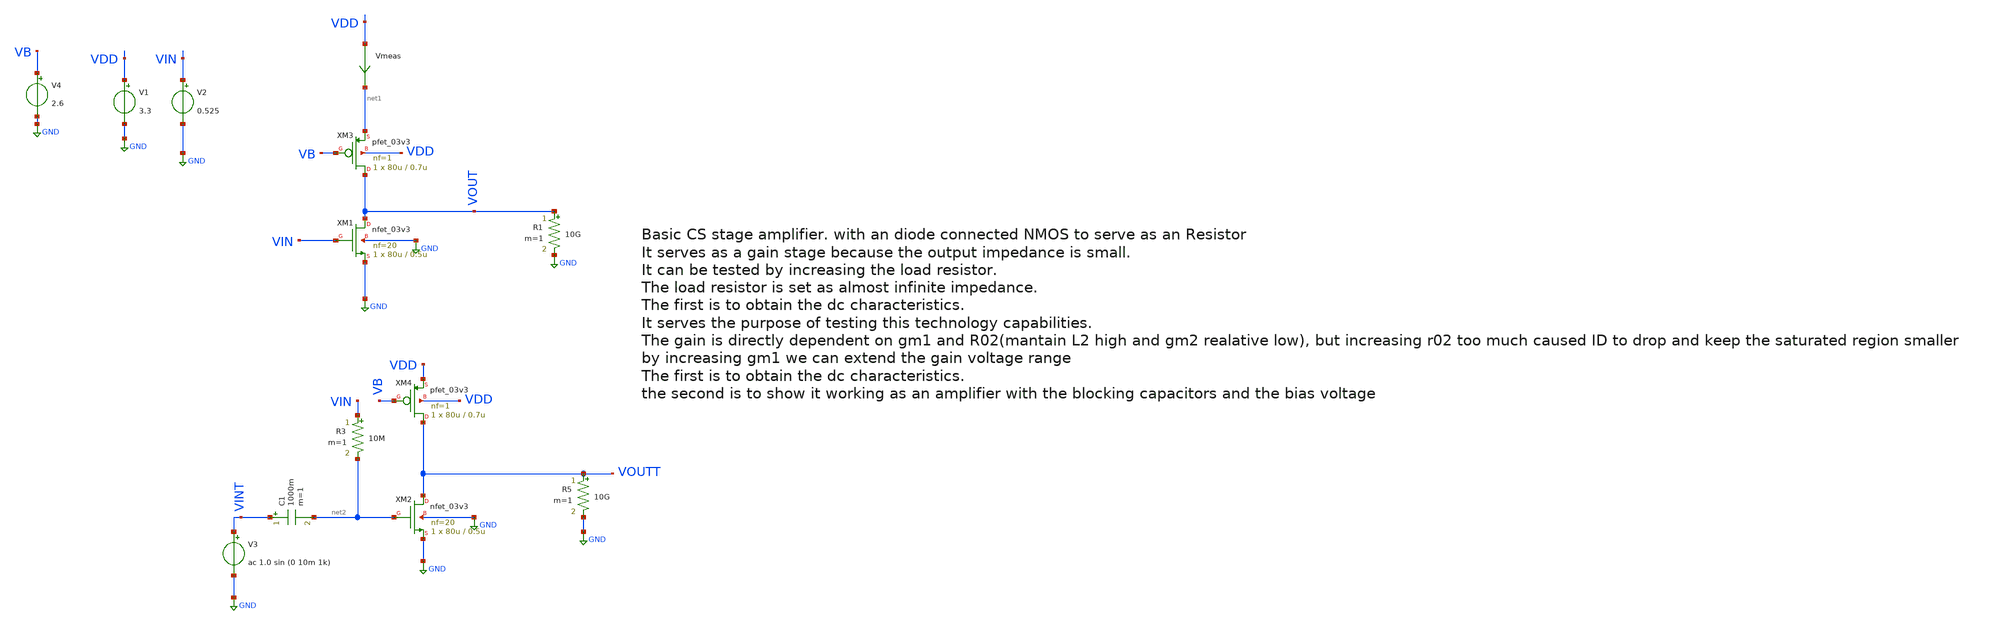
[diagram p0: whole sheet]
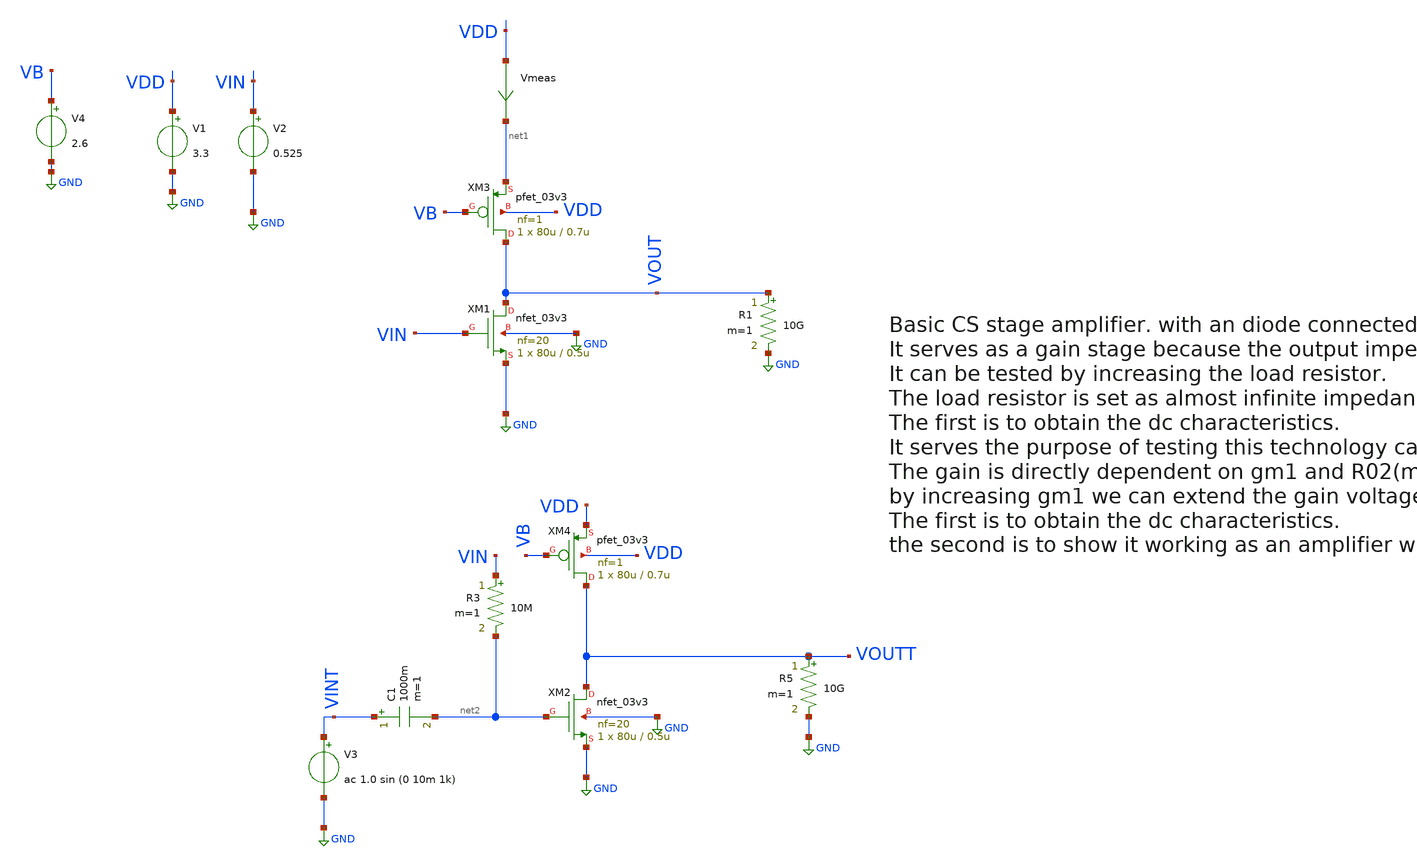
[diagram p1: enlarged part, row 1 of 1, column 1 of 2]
** sch_path: basic_circuits/cs_current_source_stage.sch
**.subckt cs_current_source_stage
XM1 VOUT VIN GND GND nfet_03v3 L=0.5u W=80u nf=20 ad='int((nf+1)/2) * W/nf * 0.18u' as='int((nf+2)/2) * W/nf * 0.18u'
+ pd='2*int((nf+1)/2) * (W/nf + 0.18u)' ps='2*int((nf+2)/2) * (W/nf + 0.18u)' nrd='0.18u / W' nrs='0.18u / W'
+ sa=0 sb=0 sd=0 m=1
Vmeas VDD net1 0
.save i(vmeas)
V1 VDD GND 3.3
V2 VIN GND 0.525
V3 VINT GND ac 1.0 sin (0 10m 1k)
C1 VINT net2 1000m m=1
R3 VIN net2 10M m=1
R5 VOUTT GND 10G m=1
XM2 VOUTT net2 GND GND nfet_03v3 L=0.5u W=80u nf=20 ad='int((nf+1)/2) * W/nf * 0.18u' as='int((nf+2)/2) * W/nf * 0.18u'
+ pd='2*int((nf+1)/2) * (W/nf + 0.18u)' ps='2*int((nf+2)/2) * (W/nf + 0.18u)' nrd='0.18u / W' nrs='0.18u / W'
+ sa=0 sb=0 sd=0 m=1
XM3 VOUT VB net1 VDD pfet_03v3 L=0.7u W=80u nf=1 ad='int((nf+1)/2) * W/nf * 0.18u' as='int((nf+2)/2) * W/nf * 0.18u'
+ pd='2*int((nf+1)/2) * (W/nf + 0.18u)' ps='2*int((nf+2)/2) * (W/nf + 0.18u)' nrd='0.18u / W' nrs='0.18u / W'
+ sa=0 sb=0 sd=0 m=1
V4 VB GND 2.6
XM4 VOUTT VB VDD VDD pfet_03v3 L=0.7u W=80u nf=1 ad='int((nf+1)/2) * W/nf * 0.18u' as='int((nf+2)/2) * W/nf * 0.18u'
+ pd='2*int((nf+1)/2) * (W/nf + 0.18u)' ps='2*int((nf+2)/2) * (W/nf + 0.18u)' nrd='0.18u / W' nrs='0.18u / W'
+ sa=0 sb=0 sd=0 m=1
R1 VOUT GND 10G m=1
**** begin user architecture code

**************************************************************
**************************************************************
**************************************************************
**************************************************************
**************************************************************
*LIBs*********************************************************
**************************************************************
**************************************************************
**************************************************************
**************************************************************
**************************************************************
.include $::180MCU_MODELS/design.ngspice
*.lib $::180MCU_MODELS/sm141064.ngspice statistical *use statistical if you want global and parameter mismatch
*.lib $::180MCU_MODELS/sm141064.ngspice res_statistical
.lib $::180MCU_MODELS/sm141064.ngspice typical
.lib $::180MCU_MODELS/sm141064.ngspice res_typical
.lib $::180MCU_MODELS/sm141064.ngspice moscap_typical
.lib $::180MCU_MODELS/sm141064.ngspice bjt_typical
.lib $::180MCU_MODELS/sm141064.ngspice diode_typical
.lib $::180MCU_MODELS/sm141064.ngspice mimcap_typical
**************************************************************
**************************************************************
**************************************************************
**************************************************************
**************************************************************
*Corners/montecarlo options***********************************
**************************************************************
**************************************************************
**************************************************************
**************************************************************
**************************************************************
.TEMP 27
.param   sw_stat_global = 1   sw_stat_mism = 1  mc_skew = 3  res_mc_skew = 3  cap_mc_skew = 3
+  fnoicor = 1
**************************************************************
**************************************************************
**************************************************************
**************************************************************
*SIMULATION and Plots*****************************************
**************************************************************
**************************************************************
**************************************************************
**************************************************************
.control
save all
dc V2 0 3.3 0.01
*dc simulation
plot v(VOUT) v(VIN) deriv(v(VOUT))
*ploting VIN VOUT and the voltage gain
plot i(Vmeas)
*ploting the current for curiosity
tran 100ns 2m
*transient simulation
plot (v(VINT)) (v(VOUTT)-1.700)
*simple plot to exemplify the gain
fft v(VOUTT) v(VINT)
*fast fourier transfor
plot mag(v(VOUTT)) mag(v(VINT))
* analyse the frequency spectrum of the transient waves, to detect distortion
ac dec 20 1 50G
*simple ac simulation
plot v(VOUTT)
*gain in function of the input frequency
.endc

**** end user architecture code
**.ends
.GLOBAL GND
.end
